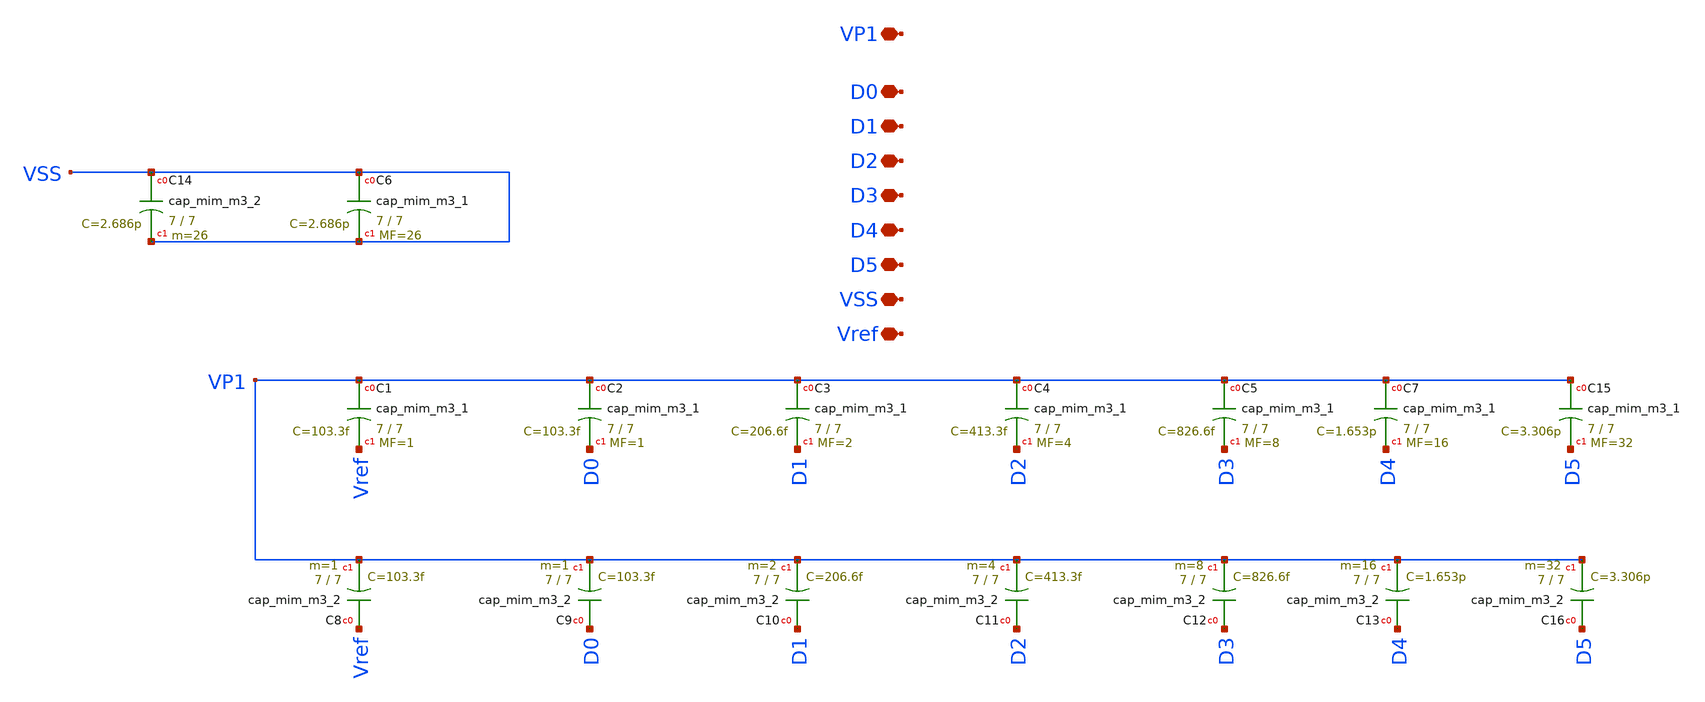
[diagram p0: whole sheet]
** sch_path: xschem/EF_LSB_CAP.sch
**.subckt EF_LSB_CAP VP1 D0 D1 D2 D3 D4 VSS D5 Vref
*.iopin VP1
*.iopin D0
*.iopin D1
*.iopin D2
*.iopin D3
*.iopin D4
*.iopin VSS
*.iopin D5
*.iopin Vref
XC1 VP1 Vref sky130_fd_pr__cap_mim_m3_1 W=7 L=7 MF=1 m=1
XC2 VP1 D0 sky130_fd_pr__cap_mim_m3_1 W=7 L=7 MF=1 m=1
XC6 VSS VSS sky130_fd_pr__cap_mim_m3_1 W=7 L=7 MF=26 m=26
XC8 Vref VP1 sky130_fd_pr__cap_mim_m3_2 W=7 L=7 MF=1 m=1
XC3 VP1 D1 sky130_fd_pr__cap_mim_m3_1 W=7 L=7 MF=2 m=2
XC4 VP1 D2 sky130_fd_pr__cap_mim_m3_1 W=7 L=7 MF=4 m=4
XC5 VP1 D3 sky130_fd_pr__cap_mim_m3_1 W=7 L=7 MF=8 m=8
XC7 VP1 D4 sky130_fd_pr__cap_mim_m3_1 W=7 L=7 MF=16 m=16
XC9 D0 VP1 sky130_fd_pr__cap_mim_m3_2 W=7 L=7 MF=1 m=1
XC10 D1 VP1 sky130_fd_pr__cap_mim_m3_2 W=7 L=7 MF=2 m=2
XC11 D2 VP1 sky130_fd_pr__cap_mim_m3_2 W=7 L=7 MF=4 m=4
XC12 D3 VP1 sky130_fd_pr__cap_mim_m3_2 W=7 L=7 MF=8 m=8
XC13 D4 VP1 sky130_fd_pr__cap_mim_m3_2 W=7 L=7 MF=16 m=16
XC14 VSS VSS sky130_fd_pr__cap_mim_m3_2 W=7 L=7 MF=26 m=26
XC15 VP1 D5 sky130_fd_pr__cap_mim_m3_1 W=7 L=7 MF=32 m=32
XC16 D5 VP1 sky130_fd_pr__cap_mim_m3_2 W=7 L=7 MF=32 m=32
**.ends
.end
